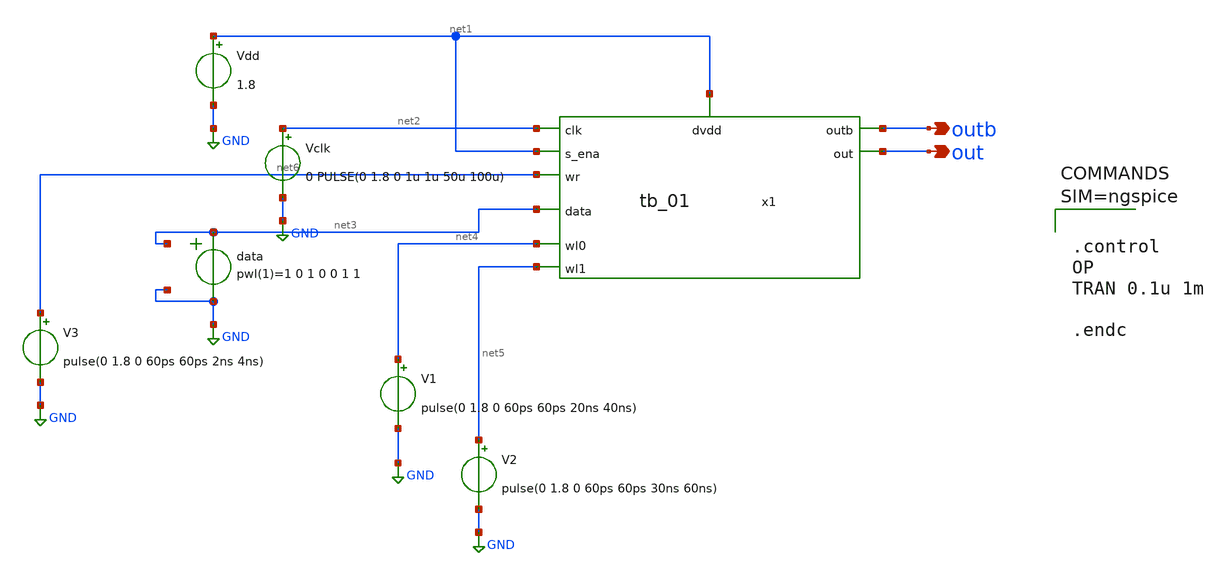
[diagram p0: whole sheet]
** sch_path: tb_2.sch
**.subckt tb_2 out outb
*.opin out
*.opin outb
Vdd net1 GND 1.8
Vclk net2 GND 0 PULSE(0 1.8 0 1u 1u 50u 100u)
data net3 GND pwl(1) net3 GND 1 0 1 0 0 1 1
V1 net4 GND pulse(0 1.8 0 60ps 60ps 20ns 40ns)
V2 net5 GND pulse(0 1.8 0 60ps 60ps 30ns 60ns)
V3 net6 GND pulse(0 1.8 0 60ps 60ps 2ns 4ns)
x1 net2 net1 net1 net6 net3 net4 outb out net5 tb_01
**** begin user architecture code



.control
OP
TRAN 0.1u 1m

.endc



.lib /usr/local/share/pdk/sky130A/libs.tech/ngspice/sky130.lib.spice tt
**** end user architecture code
**.ends
.GLOBAL GND
.end
